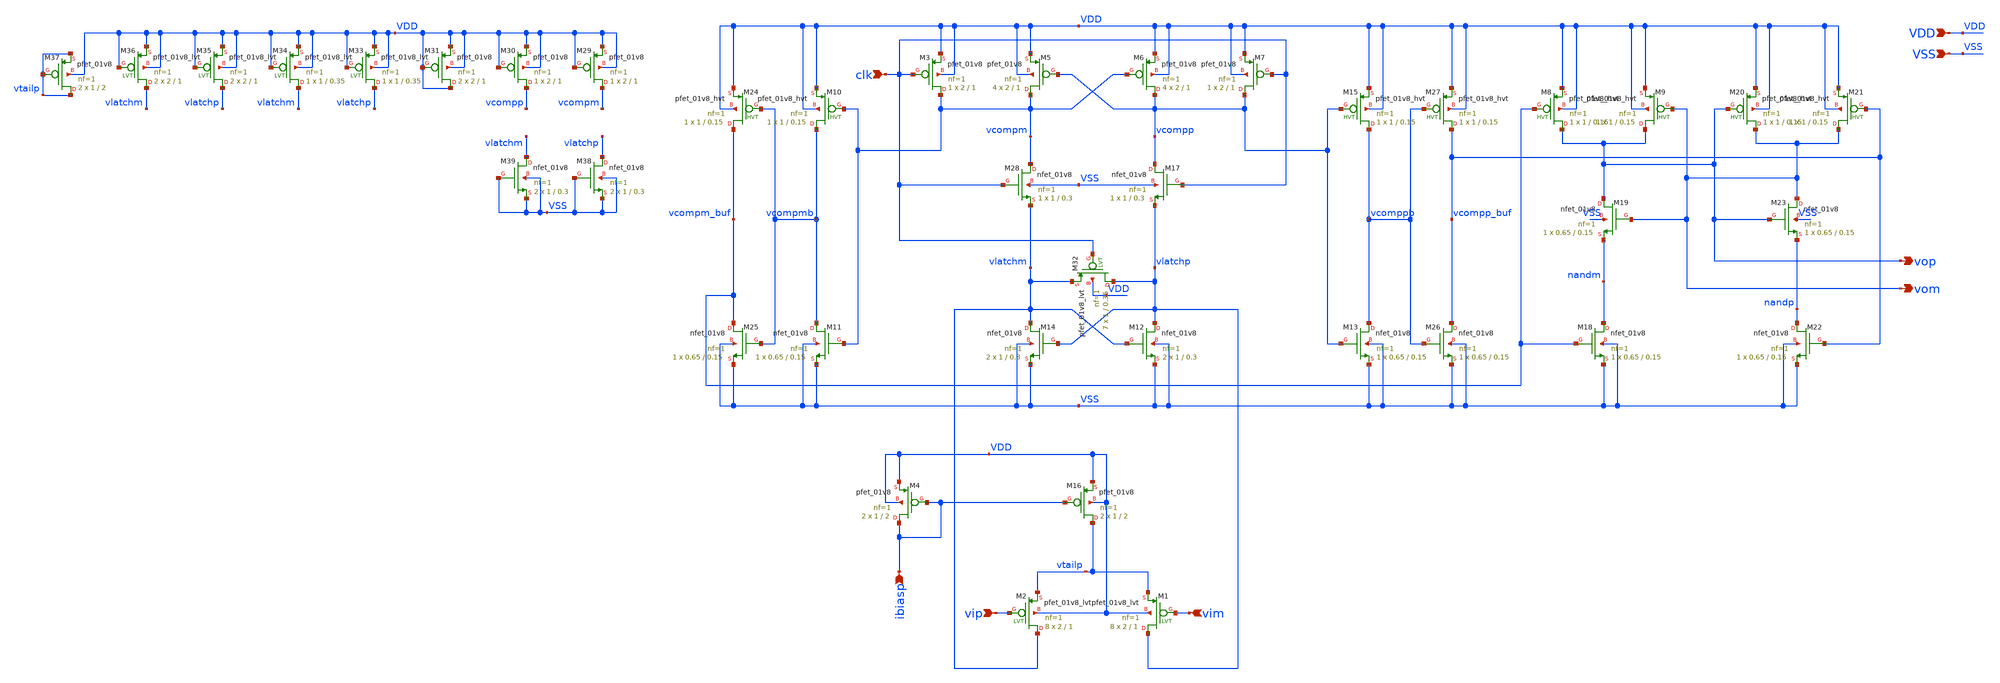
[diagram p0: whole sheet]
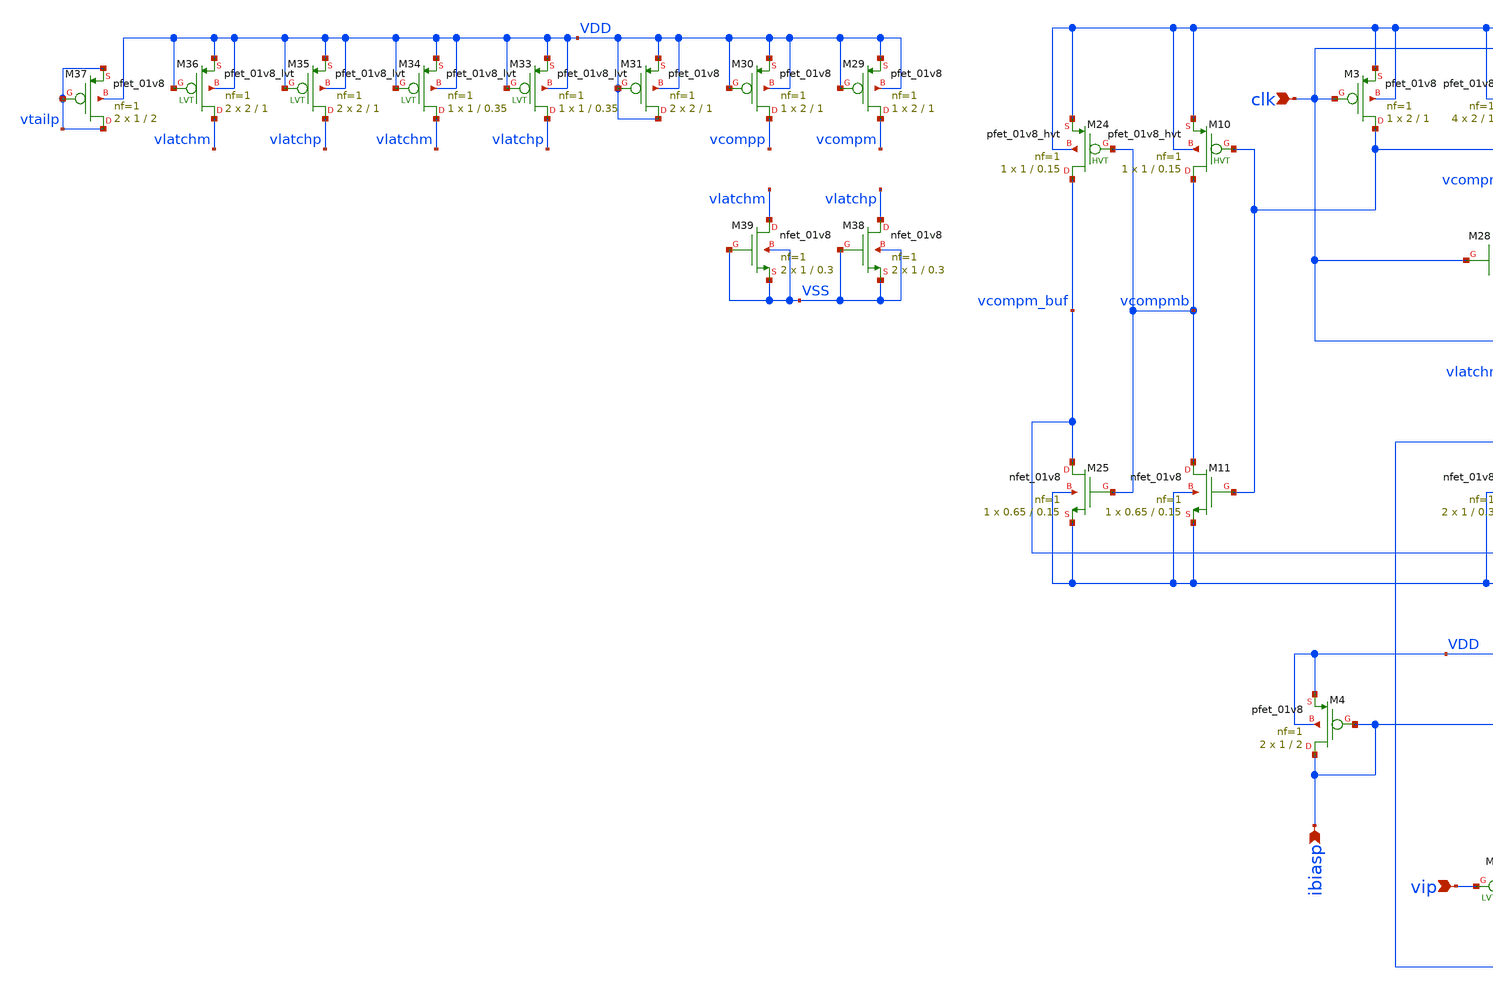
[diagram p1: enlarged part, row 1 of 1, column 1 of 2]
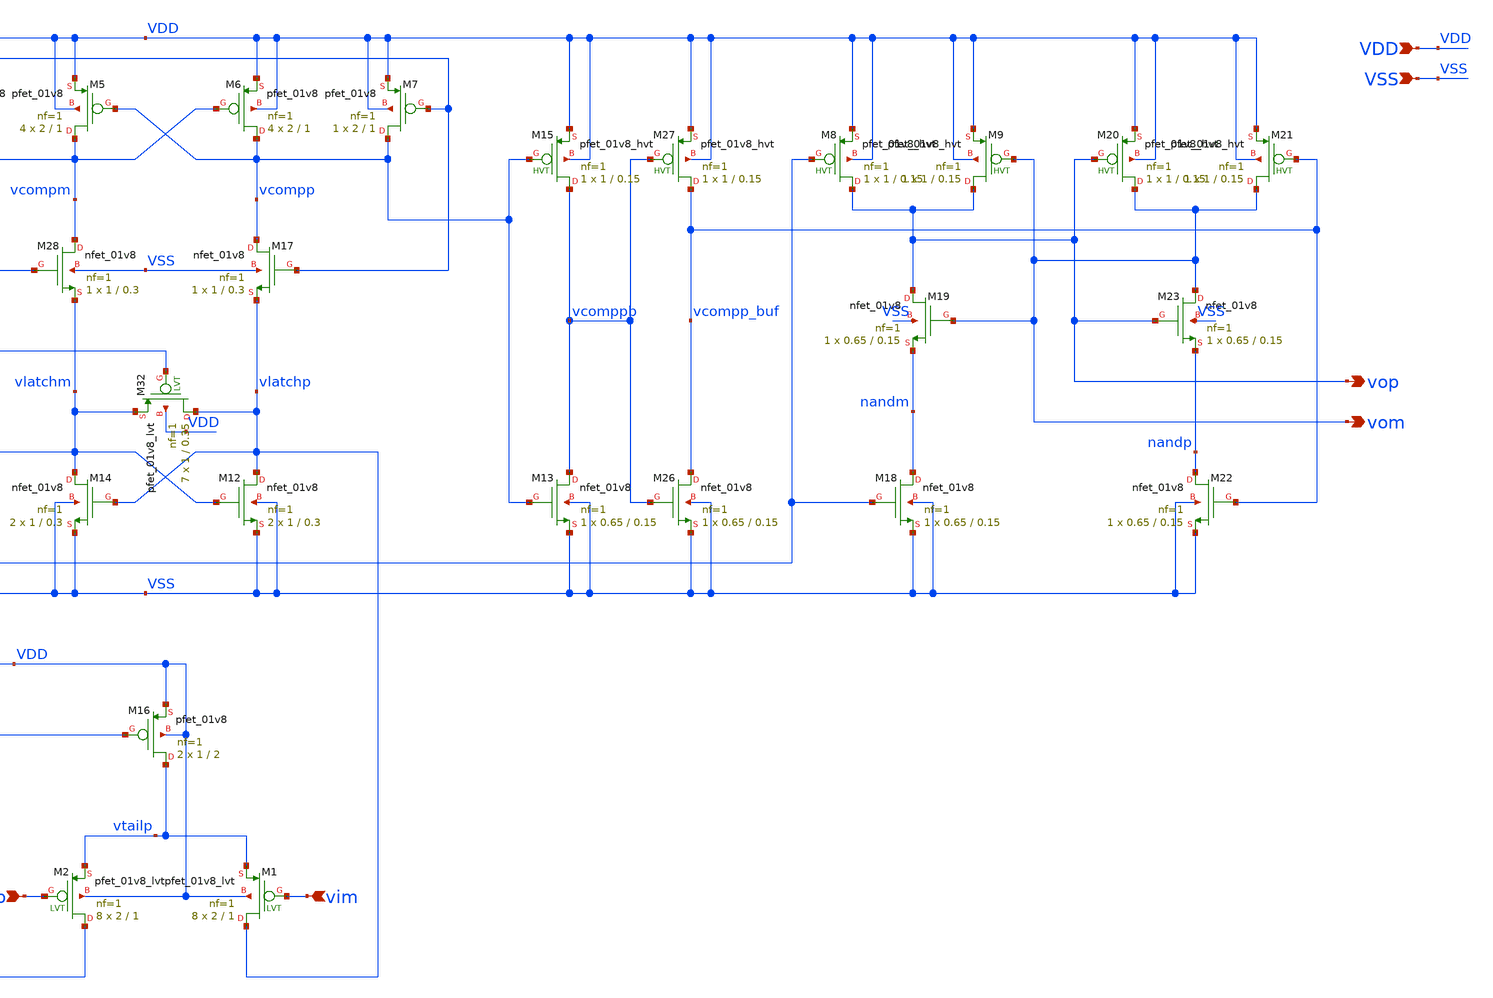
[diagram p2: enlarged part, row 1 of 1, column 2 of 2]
** sch_path: designs/latched_comparator_folded_lvs.sch
**.subckt latched_comparator_folded_lvs vip vim vop vom clk ibiasp VDD VSS
*.ipin vip
*.ipin vim
*.opin vop
*.opin vom
*.ipin clk
*.ipin ibiasp
*.ipin VDD
*.ipin VSS
XM5 vcompm vcompp VDD VDD sky130_fd_pr__pfet_01v8 L=1 W=2 nf=1 ad='int((nf+1)/2) * W/nf * 0.29' as='int((nf+2)/2) * W/nf * 0.29'
+ pd='2*int((nf+1)/2) * (W/nf + 0.29)' ps='2*int((nf+2)/2) * (W/nf + 0.29)' nrd='0.29 / W' nrs='0.29 / W'
+ sa=0 sb=0 sd=0 mult=4 m=4
XM11 vcompmb vcompm VSS VSS sky130_fd_pr__nfet_01v8 L=0.15 W=0.65 nf=1 ad='int((nf+1)/2) * W/nf * 0.29'
+ as='int((nf+2)/2) * W/nf * 0.29' pd='2*int((nf+1)/2) * (W/nf + 0.29)' ps='2*int((nf+2)/2) * (W/nf + 0.29)'
+ nrd='0.29 / W' nrs='0.29 / W' sa=0 sb=0 sd=0 mult=1 m=1
XM13 vcomppb vcompp VSS VSS sky130_fd_pr__nfet_01v8 L=0.15 W=0.65 nf=1 ad='int((nf+1)/2) * W/nf * 0.29'
+ as='int((nf+2)/2) * W/nf * 0.29' pd='2*int((nf+1)/2) * (W/nf + 0.29)' ps='2*int((nf+2)/2) * (W/nf + 0.29)'
+ nrd='0.29 / W' nrs='0.29 / W' sa=0 sb=0 sd=0 mult=1 m=1
XM15 vcomppb vcompp VDD VDD sky130_fd_pr__pfet_01v8_hvt L=0.15 W=1 nf=1 ad='int((nf+1)/2) * W/nf * 0.29'
+ as='int((nf+2)/2) * W/nf * 0.29' pd='2*int((nf+1)/2) * (W/nf + 0.29)' ps='2*int((nf+2)/2) * (W/nf + 0.29)'
+ nrd='0.29 / W' nrs='0.29 / W' sa=0 sb=0 sd=0 mult=1 m=1
XM6 vcompp vcompm VDD VDD sky130_fd_pr__pfet_01v8 L=1 W=2 nf=1 ad='int((nf+1)/2) * W/nf * 0.29' as='int((nf+2)/2) * W/nf * 0.29'
+ pd='2*int((nf+1)/2) * (W/nf + 0.29)' ps='2*int((nf+2)/2) * (W/nf + 0.29)' nrd='0.29 / W' nrs='0.29 / W'
+ sa=0 sb=0 sd=0 mult=4 m=4
XM14 vlatchm vlatchp VSS VSS sky130_fd_pr__nfet_01v8 L=0.3 W=1 nf=1 ad='int((nf+1)/2) * W/nf * 0.29'
+ as='int((nf+2)/2) * W/nf * 0.29' pd='2*int((nf+1)/2) * (W/nf + 0.29)' ps='2*int((nf+2)/2) * (W/nf + 0.29)'
+ nrd='0.29 / W' nrs='0.29 / W' sa=0 sb=0 sd=0 mult=2 m=2
XM3 vcompm clk VDD VDD sky130_fd_pr__pfet_01v8 L=1 W=2 nf=1 ad='int((nf+1)/2) * W/nf * 0.29' as='int((nf+2)/2) * W/nf * 0.29'
+ pd='2*int((nf+1)/2) * (W/nf + 0.29)' ps='2*int((nf+2)/2) * (W/nf + 0.29)' nrd='0.29 / W' nrs='0.29 / W'
+ sa=0 sb=0 sd=0 mult=1 m=1
XM7 vcompp clk VDD VDD sky130_fd_pr__pfet_01v8 L=1 W=2 nf=1 ad='int((nf+1)/2) * W/nf * 0.29' as='int((nf+2)/2) * W/nf * 0.29'
+ pd='2*int((nf+1)/2) * (W/nf + 0.29)' ps='2*int((nf+2)/2) * (W/nf + 0.29)' nrd='0.29 / W' nrs='0.29 / W'
+ sa=0 sb=0 sd=0 mult=1 m=1
XM8 vop vcompm_buf VDD VDD sky130_fd_pr__pfet_01v8_hvt L=0.15 W=1 nf=1 ad='int((nf+1)/2) * W/nf * 0.29'
+ as='int((nf+2)/2) * W/nf * 0.29' pd='2*int((nf+1)/2) * (W/nf + 0.29)' ps='2*int((nf+2)/2) * (W/nf + 0.29)'
+ nrd='0.29 / W' nrs='0.29 / W' sa=0 sb=0 sd=0 mult=1 m=1
XM9 vop vom VDD VDD sky130_fd_pr__pfet_01v8_hvt L=0.15 W=1 nf=1 ad='int((nf+1)/2) * W/nf * 0.29' as='int((nf+2)/2) * W/nf * 0.29'
+ pd='2*int((nf+1)/2) * (W/nf + 0.29)' ps='2*int((nf+2)/2) * (W/nf + 0.29)' nrd='0.29 / W' nrs='0.29 / W'
+ sa=0 sb=0 sd=0 mult=1 m=1
XM18 nandm vcompm_buf VSS VSS sky130_fd_pr__nfet_01v8 L=0.15 W=0.65 nf=1 ad='int((nf+1)/2) * W/nf * 0.29'
+ as='int((nf+2)/2) * W/nf * 0.29' pd='2*int((nf+1)/2) * (W/nf + 0.29)' ps='2*int((nf+2)/2) * (W/nf + 0.29)'
+ nrd='0.29 / W' nrs='0.29 / W' sa=0 sb=0 sd=0 mult=1 m=1
XM19 vop vom nandm VSS sky130_fd_pr__nfet_01v8 L=0.15 W=0.65 nf=1 ad='int((nf+1)/2) * W/nf * 0.29' as='int((nf+2)/2) * W/nf * 0.29'
+ pd='2*int((nf+1)/2) * (W/nf + 0.29)' ps='2*int((nf+2)/2) * (W/nf + 0.29)' nrd='0.29 / W' nrs='0.29 / W'
+ sa=0 sb=0 sd=0 mult=1 m=1
XM20 vom vop VDD VDD sky130_fd_pr__pfet_01v8_hvt L=0.15 W=1 nf=1 ad='int((nf+1)/2) * W/nf * 0.29' as='int((nf+2)/2) * W/nf * 0.29'
+ pd='2*int((nf+1)/2) * (W/nf + 0.29)' ps='2*int((nf+2)/2) * (W/nf + 0.29)' nrd='0.29 / W' nrs='0.29 / W'
+ sa=0 sb=0 sd=0 mult=1 m=1
XM21 vom vcompp_buf VDD VDD sky130_fd_pr__pfet_01v8_hvt L=0.15 W=1 nf=1 ad='int((nf+1)/2) * W/nf * 0.29'
+ as='int((nf+2)/2) * W/nf * 0.29' pd='2*int((nf+1)/2) * (W/nf + 0.29)' ps='2*int((nf+2)/2) * (W/nf + 0.29)'
+ nrd='0.29 / W' nrs='0.29 / W' sa=0 sb=0 sd=0 mult=1 m=1
XM22 nandp vcompp_buf VSS VSS sky130_fd_pr__nfet_01v8 L=0.15 W=0.65 nf=1 ad='int((nf+1)/2) * W/nf * 0.29'
+ as='int((nf+2)/2) * W/nf * 0.29' pd='2*int((nf+1)/2) * (W/nf + 0.29)' ps='2*int((nf+2)/2) * (W/nf + 0.29)'
+ nrd='0.29 / W' nrs='0.29 / W' sa=0 sb=0 sd=0 mult=1 m=1
XM23 vom vop nandp VSS sky130_fd_pr__nfet_01v8 L=0.15 W=0.65 nf=1 ad='int((nf+1)/2) * W/nf * 0.29' as='int((nf+2)/2) * W/nf * 0.29'
+ pd='2*int((nf+1)/2) * (W/nf + 0.29)' ps='2*int((nf+2)/2) * (W/nf + 0.29)' nrd='0.29 / W' nrs='0.29 / W'
+ sa=0 sb=0 sd=0 mult=1 m=1
XM25 vcompm_buf vcompmb VSS VSS sky130_fd_pr__nfet_01v8 L=0.15 W=0.65 nf=1 ad='int((nf+1)/2) * W/nf * 0.29'
+ as='int((nf+2)/2) * W/nf * 0.29' pd='2*int((nf+1)/2) * (W/nf + 0.29)' ps='2*int((nf+2)/2) * (W/nf + 0.29)'
+ nrd='0.29 / W' nrs='0.29 / W' sa=0 sb=0 sd=0 mult=1 m=1
XM26 vcompp_buf vcomppb VSS VSS sky130_fd_pr__nfet_01v8 L=0.15 W=0.65 nf=1 ad='int((nf+1)/2) * W/nf * 0.29'
+ as='int((nf+2)/2) * W/nf * 0.29' pd='2*int((nf+1)/2) * (W/nf + 0.29)' ps='2*int((nf+2)/2) * (W/nf + 0.29)'
+ nrd='0.29 / W' nrs='0.29 / W' sa=0 sb=0 sd=0 mult=1 m=1
XM27 vcompp_buf vcomppb VDD VDD sky130_fd_pr__pfet_01v8_hvt L=0.15 W=1 nf=1 ad='int((nf+1)/2) * W/nf * 0.29'
+ as='int((nf+2)/2) * W/nf * 0.29' pd='2*int((nf+1)/2) * (W/nf + 0.29)' ps='2*int((nf+2)/2) * (W/nf + 0.29)'
+ nrd='0.29 / W' nrs='0.29 / W' sa=0 sb=0 sd=0 mult=1 m=1
XM4 ibiasp ibiasp VDD VDD sky130_fd_pr__pfet_01v8 L=2 W=1 nf=1 ad='int((nf+1)/2) * W/nf * 0.29' as='int((nf+2)/2) * W/nf * 0.29'
+ pd='2*int((nf+1)/2) * (W/nf + 0.29)' ps='2*int((nf+2)/2) * (W/nf + 0.29)' nrd='0.29 / W' nrs='0.29 / W'
+ sa=0 sb=0 sd=0 mult=2 m=2
XM2 vlatchm vip vtailp VDD sky130_fd_pr__pfet_01v8_lvt L=1 W=2 nf=1 ad='int((nf+1)/2) * W/nf * 0.29'
+ as='int((nf+2)/2) * W/nf * 0.29' pd='2*int((nf+1)/2) * (W/nf + 0.29)' ps='2*int((nf+2)/2) * (W/nf + 0.29)'
+ nrd='0.29 / W' nrs='0.29 / W' sa=0 sb=0 sd=0 mult=8 m=8
XM1 vlatchp vim vtailp VDD sky130_fd_pr__pfet_01v8_lvt L=1 W=2 nf=1 ad='int((nf+1)/2) * W/nf * 0.29'
+ as='int((nf+2)/2) * W/nf * 0.29' pd='2*int((nf+1)/2) * (W/nf + 0.29)' ps='2*int((nf+2)/2) * (W/nf + 0.29)'
+ nrd='0.29 / W' nrs='0.29 / W' sa=0 sb=0 sd=0 mult=8 m=8
XM32 vlatchp clk vlatchm VDD sky130_fd_pr__pfet_01v8_lvt L=0.35 W=1 nf=1 ad='int((nf+1)/2) * W/nf * 0.29'
+ as='int((nf+2)/2) * W/nf * 0.29' pd='2*int((nf+1)/2) * (W/nf + 0.29)' ps='2*int((nf+2)/2) * (W/nf + 0.29)'
+ nrd='0.29 / W' nrs='0.29 / W' sa=0 sb=0 sd=0 mult=7 m=7
XM16 vtailp ibiasp VDD VDD sky130_fd_pr__pfet_01v8 L=2 W=1 nf=1 ad='int((nf+1)/2) * W/nf * 0.29' as='int((nf+2)/2) * W/nf * 0.29'
+ pd='2*int((nf+1)/2) * (W/nf + 0.29)' ps='2*int((nf+2)/2) * (W/nf + 0.29)' nrd='0.29 / W' nrs='0.29 / W'
+ sa=0 sb=0 sd=0 mult=2 m=2
XM12 vlatchp vlatchm VSS VSS sky130_fd_pr__nfet_01v8 L=0.3 W=1 nf=1 ad='int((nf+1)/2) * W/nf * 0.29'
+ as='int((nf+2)/2) * W/nf * 0.29' pd='2*int((nf+1)/2) * (W/nf + 0.29)' ps='2*int((nf+2)/2) * (W/nf + 0.29)'
+ nrd='0.29 / W' nrs='0.29 / W' sa=0 sb=0 sd=0 mult=2 m=2
XM17 vcompp clk vlatchp VSS sky130_fd_pr__nfet_01v8 L=0.3 W=1 nf=1 ad='int((nf+1)/2) * W/nf * 0.29' as='int((nf+2)/2) * W/nf * 0.29'
+ pd='2*int((nf+1)/2) * (W/nf + 0.29)' ps='2*int((nf+2)/2) * (W/nf + 0.29)' nrd='0.29 / W' nrs='0.29 / W'
+ sa=0 sb=0 sd=0 mult=1 m=1
XM28 vcompm clk vlatchm VSS sky130_fd_pr__nfet_01v8 L=0.3 W=1 nf=1 ad='int((nf+1)/2) * W/nf * 0.29' as='int((nf+2)/2) * W/nf * 0.29'
+ pd='2*int((nf+1)/2) * (W/nf + 0.29)' ps='2*int((nf+2)/2) * (W/nf + 0.29)' nrd='0.29 / W' nrs='0.29 / W'
+ sa=0 sb=0 sd=0 mult=1 m=1
XM24 vcompm_buf vcompmb VDD VDD sky130_fd_pr__pfet_01v8_hvt L=0.15 W=1 nf=1 ad='int((nf+1)/2) * W/nf * 0.29'
+ as='int((nf+2)/2) * W/nf * 0.29' pd='2*int((nf+1)/2) * (W/nf + 0.29)' ps='2*int((nf+2)/2) * (W/nf + 0.29)'
+ nrd='0.29 / W' nrs='0.29 / W' sa=0 sb=0 sd=0 mult=1 m=1
XM10 vcompmb vcompm VDD VDD sky130_fd_pr__pfet_01v8_hvt L=0.15 W=1 nf=1 ad='int((nf+1)/2) * W/nf * 0.29'
+ as='int((nf+2)/2) * W/nf * 0.29' pd='2*int((nf+1)/2) * (W/nf + 0.29)' ps='2*int((nf+2)/2) * (W/nf + 0.29)'
+ nrd='0.29 / W' nrs='0.29 / W' sa=0 sb=0 sd=0 mult=1 m=1
XM29 vcompm VDD VDD VDD sky130_fd_pr__pfet_01v8 L=1 W=2 nf=1 ad='int((nf+1)/2) * W/nf * 0.29' as='int((nf+2)/2) * W/nf * 0.29'
+ pd='2*int((nf+1)/2) * (W/nf + 0.29)' ps='2*int((nf+2)/2) * (W/nf + 0.29)' nrd='0.29 / W' nrs='0.29 / W'
+ sa=0 sb=0 sd=0 mult=1 m=1
XM30 vcompp VDD VDD VDD sky130_fd_pr__pfet_01v8 L=1 W=2 nf=1 ad='int((nf+1)/2) * W/nf * 0.29' as='int((nf+2)/2) * W/nf * 0.29'
+ pd='2*int((nf+1)/2) * (W/nf + 0.29)' ps='2*int((nf+2)/2) * (W/nf + 0.29)' nrd='0.29 / W' nrs='0.29 / W'
+ sa=0 sb=0 sd=0 mult=1 m=1
XM31 VDD VDD VDD VDD sky130_fd_pr__pfet_01v8 L=1 W=2 nf=1 ad='int((nf+1)/2) * W/nf * 0.29' as='int((nf+2)/2) * W/nf * 0.29'
+ pd='2*int((nf+1)/2) * (W/nf + 0.29)' ps='2*int((nf+2)/2) * (W/nf + 0.29)' nrd='0.29 / W' nrs='0.29 / W'
+ sa=0 sb=0 sd=0 mult=2 m=2
XM33 vlatchp VDD VDD VDD sky130_fd_pr__pfet_01v8_lvt L=0.35 W=1 nf=1 ad='int((nf+1)/2) * W/nf * 0.29'
+ as='int((nf+2)/2) * W/nf * 0.29' pd='2*int((nf+1)/2) * (W/nf + 0.29)' ps='2*int((nf+2)/2) * (W/nf + 0.29)'
+ nrd='0.29 / W' nrs='0.29 / W' sa=0 sb=0 sd=0 mult=1 m=1
XM34 vlatchm VDD VDD VDD sky130_fd_pr__pfet_01v8_lvt L=0.35 W=1 nf=1 ad='int((nf+1)/2) * W/nf * 0.29'
+ as='int((nf+2)/2) * W/nf * 0.29' pd='2*int((nf+1)/2) * (W/nf + 0.29)' ps='2*int((nf+2)/2) * (W/nf + 0.29)'
+ nrd='0.29 / W' nrs='0.29 / W' sa=0 sb=0 sd=0 mult=1 m=1
XM35 vlatchp VDD VDD VDD sky130_fd_pr__pfet_01v8_lvt L=1 W=2 nf=1 ad='int((nf+1)/2) * W/nf * 0.29' as='int((nf+2)/2) * W/nf * 0.29'
+ pd='2*int((nf+1)/2) * (W/nf + 0.29)' ps='2*int((nf+2)/2) * (W/nf + 0.29)' nrd='0.29 / W' nrs='0.29 / W'
+ sa=0 sb=0 sd=0 mult=2 m=2
XM36 vlatchm VDD VDD VDD sky130_fd_pr__pfet_01v8_lvt L=1 W=2 nf=1 ad='int((nf+1)/2) * W/nf * 0.29' as='int((nf+2)/2) * W/nf * 0.29'
+ pd='2*int((nf+1)/2) * (W/nf + 0.29)' ps='2*int((nf+2)/2) * (W/nf + 0.29)' nrd='0.29 / W' nrs='0.29 / W'
+ sa=0 sb=0 sd=0 mult=2 m=2
XM37 vtailp vtailp vtailp VDD sky130_fd_pr__pfet_01v8 L=2 W=1 nf=1 ad='int((nf+1)/2) * W/nf * 0.29' as='int((nf+2)/2) * W/nf * 0.29'
+ pd='2*int((nf+1)/2) * (W/nf + 0.29)' ps='2*int((nf+2)/2) * (W/nf + 0.29)' nrd='0.29 / W' nrs='0.29 / W'
+ sa=0 sb=0 sd=0 mult=2 m=2
XM38 vlatchp VSS VSS VSS sky130_fd_pr__nfet_01v8 L=0.3 W=1 nf=1 ad='int((nf+1)/2) * W/nf * 0.29' as='int((nf+2)/2) * W/nf * 0.29'
+ pd='2*int((nf+1)/2) * (W/nf + 0.29)' ps='2*int((nf+2)/2) * (W/nf + 0.29)' nrd='0.29 / W' nrs='0.29 / W'
+ sa=0 sb=0 sd=0 mult=2 m=2
XM39 vlatchm VSS VSS VSS sky130_fd_pr__nfet_01v8 L=0.3 W=1 nf=1 ad='int((nf+1)/2) * W/nf * 0.29' as='int((nf+2)/2) * W/nf * 0.29'
+ pd='2*int((nf+1)/2) * (W/nf + 0.29)' ps='2*int((nf+2)/2) * (W/nf + 0.29)' nrd='0.29 / W' nrs='0.29 / W'
+ sa=0 sb=0 sd=0 mult=2 m=2
**.ends
.end
